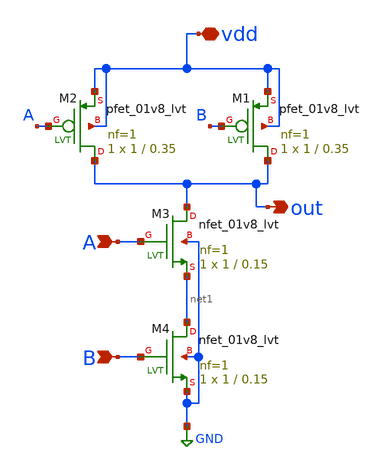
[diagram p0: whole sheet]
** sch_path: designs/subcells/core_nand/nand.sch
**.subckt nand vdd out A B
*.iopin vdd
*.opin out
*.ipin A
*.ipin B
XM4 net1 B GND GND sky130_fd_pr__nfet_01v8_lvt L=0.15 W=1 nf=1 ad='int((1 + 1)/2) * 1 / 1 * 0.29' as='int((1 + 2)/2) * 1 / 1 * 0.29'
+ pd='2*int((1 + 1)/2) * (1 / 1 + 0.29)' ps='2*int((1 + 2)/2) * (1 / 1 + 0.29)' nrd='0.29 / 1 ' nrs='0.29 / 1 '
+ sa=0 sb=0 sd=0 mult=1 m=1
XM1 out B vdd vdd sky130_fd_pr__pfet_01v8_lvt L=0.35 W=1 nf=1 ad='int((1 + 1)/2) * 1 / 1 * 0.29' as='int((1 + 2)/2) * 1 / 1 * 0.29'
+ pd='2*int((1 + 1)/2) * (1 / 1 + 0.29)' ps='2*int((1 + 2)/2) * (1 / 1 + 0.29)' nrd='0.29 / 1 ' nrs='0.29 / 1 '
+ sa=0 sb=0 sd=0 mult=1 m=1
XM2 out A vdd vdd sky130_fd_pr__pfet_01v8_lvt L=0.35 W=1 nf=1 ad='int((1 + 1)/2) * 1 / 1 * 0.29' as='int((1 + 2)/2) * 1 / 1 * 0.29'
+ pd='2*int((1 + 1)/2) * (1 / 1 + 0.29)' ps='2*int((1 + 2)/2) * (1 / 1 + 0.29)' nrd='0.29 / 1 ' nrs='0.29 / 1 '
+ sa=0 sb=0 sd=0 mult=1 m=1
XM3 out A net1 GND sky130_fd_pr__nfet_01v8_lvt L=0.15 W=1 nf=1 ad='int((1 + 1)/2) * 1 / 1 * 0.29' as='int((1 + 2)/2) * 1 / 1 * 0.29'
+ pd='2*int((1 + 1)/2) * (1 / 1 + 0.29)' ps='2*int((1 + 2)/2) * (1 / 1 + 0.29)' nrd='0.29 / 1 ' nrs='0.29 / 1 '
+ sa=0 sb=0 sd=0 mult=1 m=1
**.ends
.GLOBAL GND
.end
